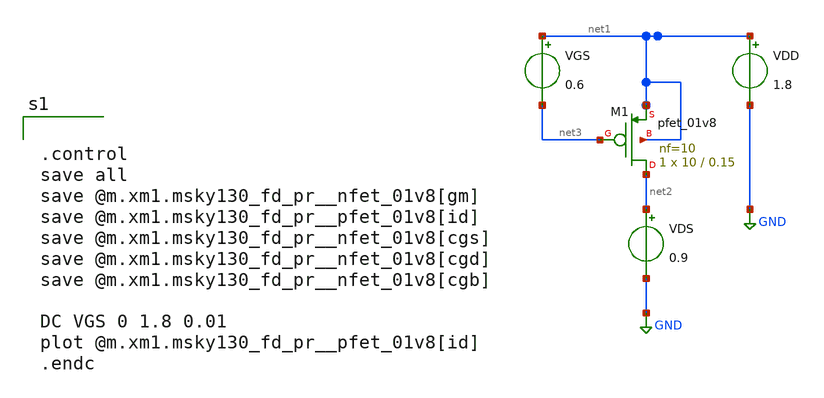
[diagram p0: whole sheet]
** sch_path: xschem/src/basic_test/ft_nmos.sch
**.subckt ft_nmos
VDD net1 GND 1.8
VGS net1 net3 0.6
VDS net2 GND 0.9
XM1 net2 net3 net1 net1 sky130_fd_pr__pfet_01v8 L=0.15 W=10 nf=10 ad='int((nf+1)/2) * W/nf * 0.29' as='int((nf+2)/2) * W/nf * 0.29'
+ pd='2*int((nf+1)/2) * (W/nf + 0.29)' ps='2*int((nf+2)/2) * (W/nf + 0.29)' nrd='0.29 / W' nrs='0.29 / W'
+ sa=0 sb=0 sd=0 mult=1 m=1
**** begin user architecture code


.control
save all
save @m.xm1.msky130_fd_pr__nfet_01v8[gm]
save @m.xm1.msky130_fd_pr__pfet_01v8[id]
save @m.xm1.msky130_fd_pr__nfet_01v8[cgs]
save @m.xm1.msky130_fd_pr__nfet_01v8[cgd]
save @m.xm1.msky130_fd_pr__nfet_01v8[cgb]

DC VGS 0 1.8 0.01
plot @m.xm1.msky130_fd_pr__pfet_01v8[id]
.endc



.include /home/eda/pdk/skywater-pdk/libraries/sky130_fd_pr_ngspice/latest/models/corners/ss.spice


* Resistor$::SKYWATER_MODELS/Capacitor
.include $::SKYWATER_MODELS/models/r+c/res_typical__cap_typical.spice
.include $::SKYWATER_MODELS/models/r+c/res_typical__cap_typical__lin.spice
* Special cells
.include $::SKYWATER_MODELS/models/corners/tt/specialized_cells.spice


**** end user architecture code
**.ends
.GLOBAL GND
.end
